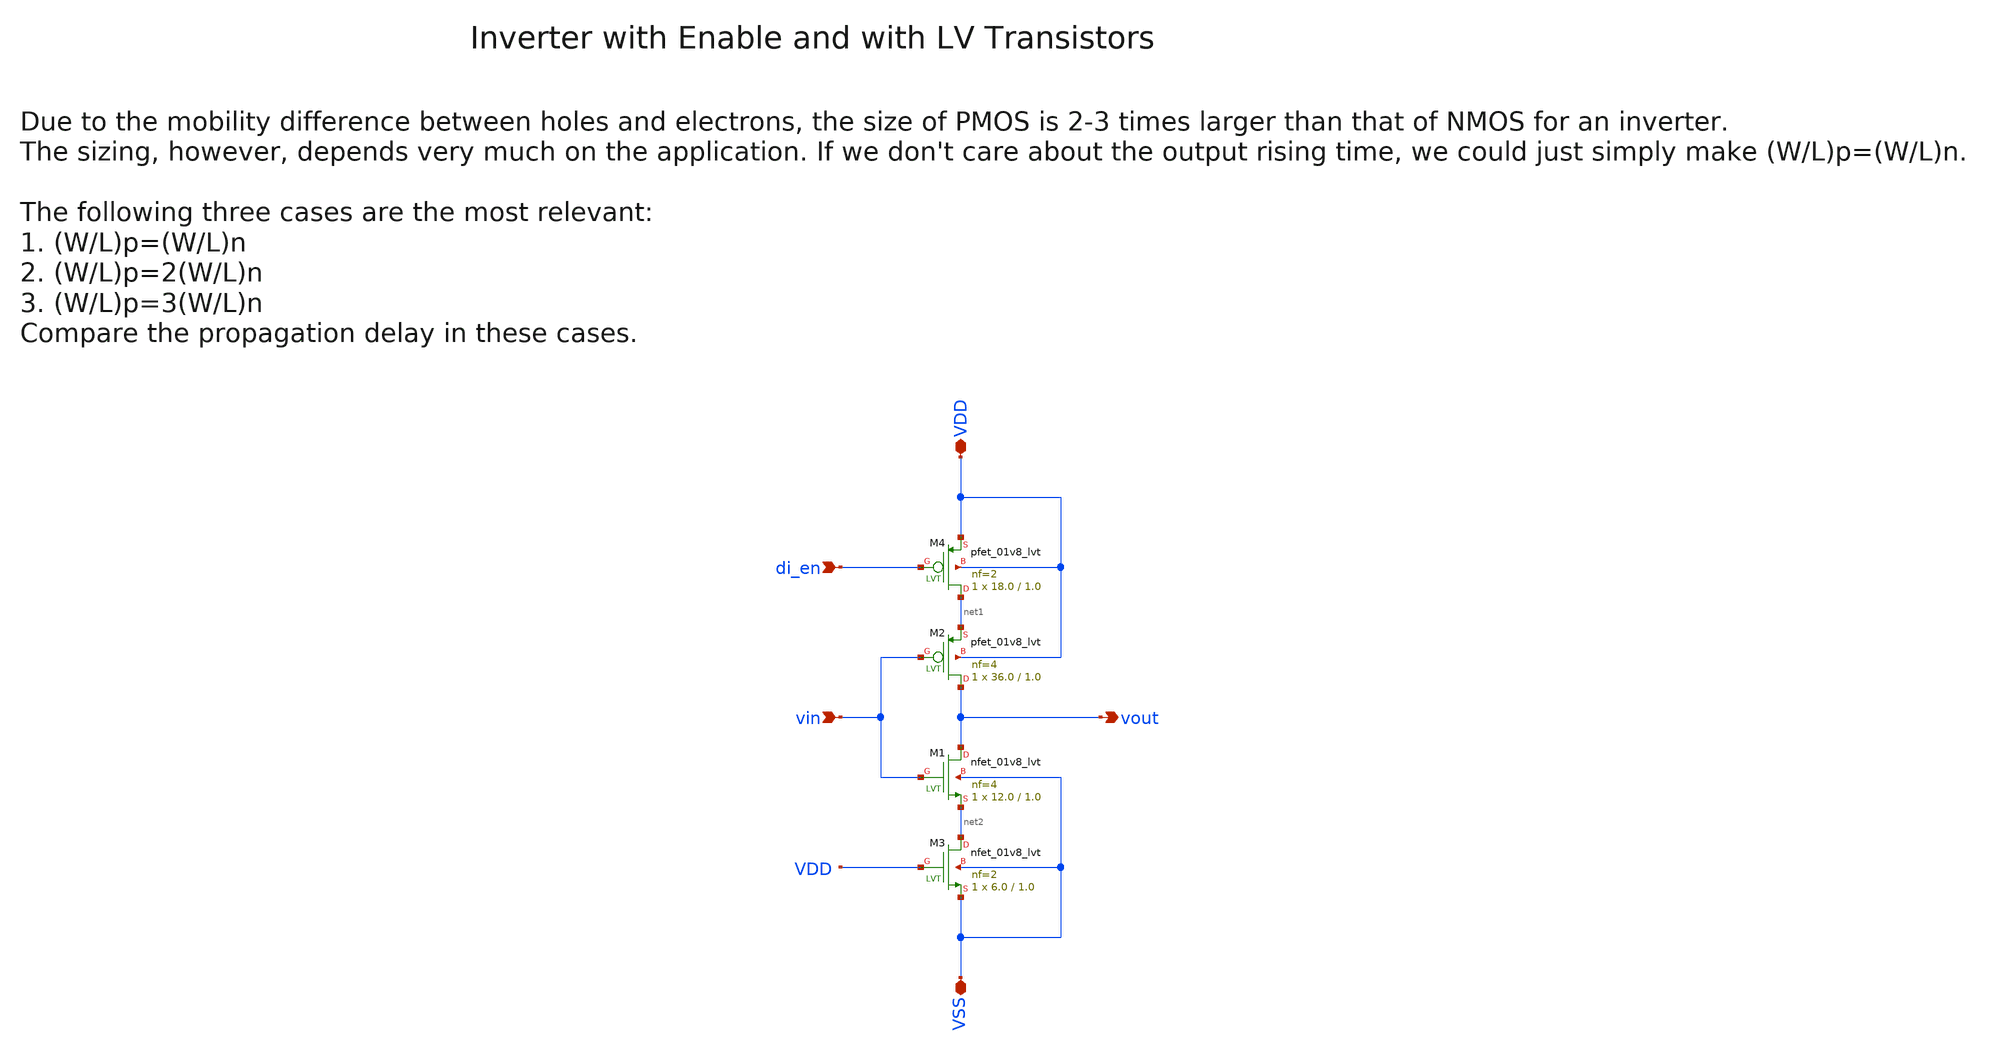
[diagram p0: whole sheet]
** sch_path: sky130/macros/iqmod/schematic/wspr_tx_iqmod_mfb_lpf_ota_core_inv_lv_en_NF4.sch
**.subckt wspr_tx_iqmod_mfb_lpf_ota_core_inv_lv_en_NF4 vin VDD VSS vout di_en
*.ipin vin
*.iopin VDD
*.iopin VSS
*.opin vout
*.ipin di_en
XM2 vout vin net1 VDD sky130_fd_pr__pfet_01v8_lvt L=1.0 W=36.0 nf=4 ad='int((4 + 1)/2) * 36.0 / 4 * 0.29'
+ as='int((4 + 2)/2) * 36.0 / 4 * 0.29' pd='2*int((4 + 1)/2) * (36.0 / 4 + 0.29)' ps='2*int((4 + 2)/2) * (36.0 / 4 + 0.29)'
+ nrd='0.29 / 36.0 ' nrs='0.29 / 36.0 ' sa=0 sb=0 sd=0 mult=1 m=1
XM3 net2 VDD VSS VSS sky130_fd_pr__nfet_01v8_lvt L=1.0 W=6.0 nf=2 ad='int((2 + 1)/2) * 6.0 / 2 * 0.29'
+ as='int((2 + 2)/2) * 6.0 / 2 * 0.29' pd='2*int((2 + 1)/2) * (6.0 / 2 + 0.29)' ps='2*int((2 + 2)/2) * (6.0 / 2 + 0.29)'
+ nrd='0.29 / 6.0 ' nrs='0.29 / 6.0 ' sa=0 sb=0 sd=0 mult=1 m=1
XM4 net1 di_en VDD VDD sky130_fd_pr__pfet_01v8_lvt L=1.0 W=18.0 nf=2 ad='int((2 + 1)/2) * 18.0 / 2 * 0.29'
+ as='int((2 + 2)/2) * 18.0 / 2 * 0.29' pd='2*int((2 + 1)/2) * (18.0 / 2 + 0.29)' ps='2*int((2 + 2)/2) * (18.0 / 2 + 0.29)'
+ nrd='0.29 / 18.0 ' nrs='0.29 / 18.0 ' sa=0 sb=0 sd=0 mult=1 m=1
XM1 vout vin net2 VSS sky130_fd_pr__nfet_01v8_lvt L=1.0 W=12.0 nf=4 ad='int((4 + 1)/2) * 12.0 / 4 * 0.29'
+ as='int((4 + 2)/2) * 12.0 / 4 * 0.29' pd='2*int((4 + 1)/2) * (12.0 / 4 + 0.29)' ps='2*int((4 + 2)/2) * (12.0 / 4 + 0.29)'
+ nrd='0.29 / 12.0 ' nrs='0.29 / 12.0 ' sa=0 sb=0 sd=0 mult=1 m=1
**.ends
.end
